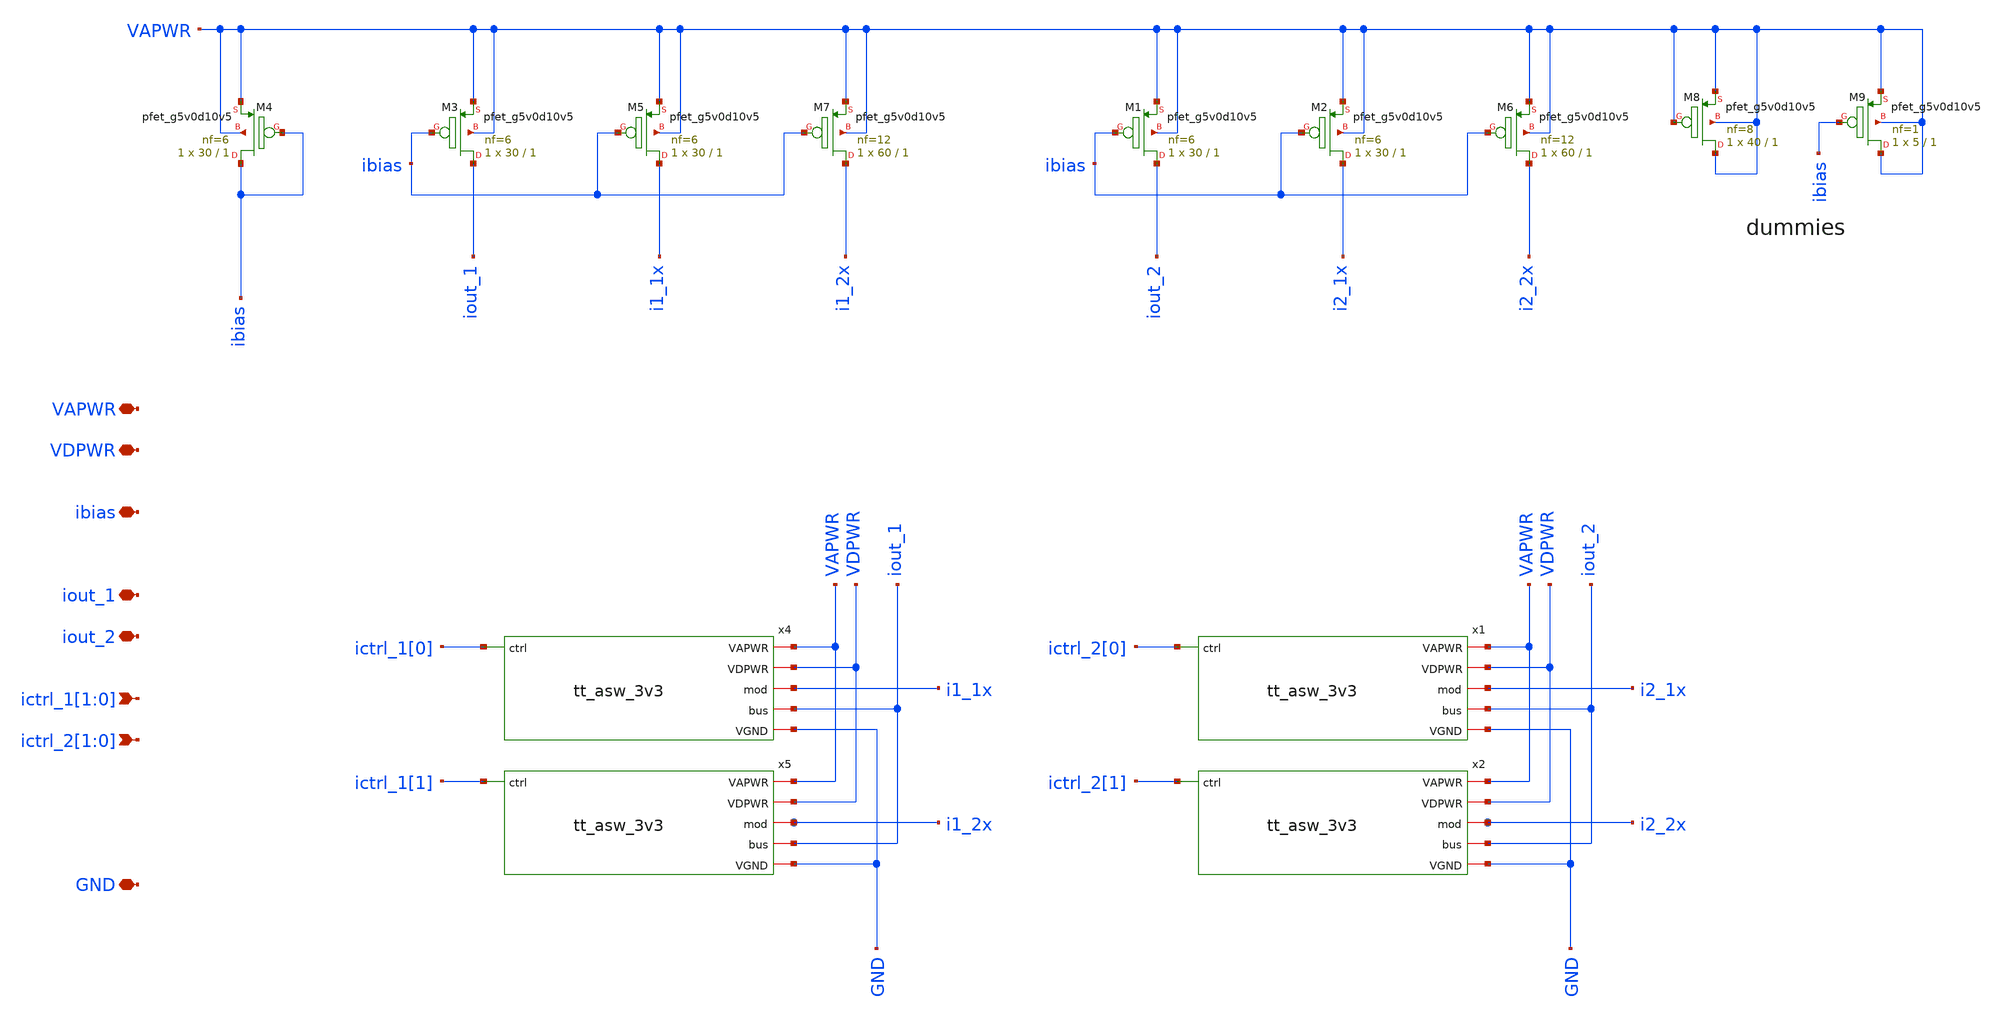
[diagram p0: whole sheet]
** sch_path: tt_um_mosbius/xschem/mirror_p.sch
**.subckt mirror_p ibias iout_1 ictrl_1[1],ictrl_1[0] ictrl_2[1],ictrl_2[0] iout_2 VAPWR VDPWR GND
*.iopin ibias
*.iopin iout_1
*.ipin ictrl_1[1],ictrl_1[0]
*.ipin ictrl_2[1],ictrl_2[0]
*.iopin iout_2
*.iopin VAPWR
*.iopin VDPWR
*.iopin GND
x4 GND VDPWR VAPWR ictrl_1[0] i1_1x iout_1 tt_asw_3v3
x5 GND VDPWR VAPWR ictrl_1[1] i1_2x iout_1 tt_asw_3v3
x1 GND VDPWR VAPWR ictrl_2[0] i2_1x iout_2 tt_asw_3v3
x2 GND VDPWR VAPWR ictrl_2[1] i2_2x iout_2 tt_asw_3v3
XM3 iout_1 ibias VAPWR VAPWR sky130_fd_pr__pfet_g5v0d10v5 L=1 W=30 nf=6 ad='int((nf+1)/2) * W/nf * 0.29'
+ as='int((nf+2)/2) * W/nf * 0.29' pd='2*int((nf+1)/2) * (W/nf + 0.29)' ps='2*int((nf+2)/2) * (W/nf + 0.29)'
+ nrd='0.29 / W' nrs='0.29 / W' sa=0 sb=0 sd=0 mult=1 m=1
XM4 ibias ibias VAPWR VAPWR sky130_fd_pr__pfet_g5v0d10v5 L=1 W=30 nf=6 ad='int((nf+1)/2) * W/nf * 0.29'
+ as='int((nf+2)/2) * W/nf * 0.29' pd='2*int((nf+1)/2) * (W/nf + 0.29)' ps='2*int((nf+2)/2) * (W/nf + 0.29)'
+ nrd='0.29 / W' nrs='0.29 / W' sa=0 sb=0 sd=0 mult=1 m=1
XM5 i1_1x ibias VAPWR VAPWR sky130_fd_pr__pfet_g5v0d10v5 L=1 W=30 nf=6 ad='int((nf+1)/2) * W/nf * 0.29'
+ as='int((nf+2)/2) * W/nf * 0.29' pd='2*int((nf+1)/2) * (W/nf + 0.29)' ps='2*int((nf+2)/2) * (W/nf + 0.29)'
+ nrd='0.29 / W' nrs='0.29 / W' sa=0 sb=0 sd=0 mult=1 m=1
XM7 i1_2x ibias VAPWR VAPWR sky130_fd_pr__pfet_g5v0d10v5 L=1 W=60 nf=12 ad='int((nf+1)/2) * W/nf * 0.29'
+ as='int((nf+2)/2) * W/nf * 0.29' pd='2*int((nf+1)/2) * (W/nf + 0.29)' ps='2*int((nf+2)/2) * (W/nf + 0.29)'
+ nrd='0.29 / W' nrs='0.29 / W' sa=0 sb=0 sd=0 mult=1 m=1
XM1 iout_2 ibias VAPWR VAPWR sky130_fd_pr__pfet_g5v0d10v5 L=1 W=30 nf=6 ad='int((nf+1)/2) * W/nf * 0.29'
+ as='int((nf+2)/2) * W/nf * 0.29' pd='2*int((nf+1)/2) * (W/nf + 0.29)' ps='2*int((nf+2)/2) * (W/nf + 0.29)'
+ nrd='0.29 / W' nrs='0.29 / W' sa=0 sb=0 sd=0 mult=1 m=1
XM2 i2_1x ibias VAPWR VAPWR sky130_fd_pr__pfet_g5v0d10v5 L=1 W=30 nf=6 ad='int((nf+1)/2) * W/nf * 0.29'
+ as='int((nf+2)/2) * W/nf * 0.29' pd='2*int((nf+1)/2) * (W/nf + 0.29)' ps='2*int((nf+2)/2) * (W/nf + 0.29)'
+ nrd='0.29 / W' nrs='0.29 / W' sa=0 sb=0 sd=0 mult=1 m=1
XM6 i2_2x ibias VAPWR VAPWR sky130_fd_pr__pfet_g5v0d10v5 L=1 W=60 nf=12 ad='int((nf+1)/2) * W/nf * 0.29'
+ as='int((nf+2)/2) * W/nf * 0.29' pd='2*int((nf+1)/2) * (W/nf + 0.29)' ps='2*int((nf+2)/2) * (W/nf + 0.29)'
+ nrd='0.29 / W' nrs='0.29 / W' sa=0 sb=0 sd=0 mult=1 m=1
XM8 VAPWR VAPWR VAPWR VAPWR sky130_fd_pr__pfet_g5v0d10v5 L=1 W=40 nf=8 ad='int((nf+1)/2) * W/nf * 0.29'
+ as='int((nf+2)/2) * W/nf * 0.29' pd='2*int((nf+1)/2) * (W/nf + 0.29)' ps='2*int((nf+2)/2) * (W/nf + 0.29)'
+ nrd='0.29 / W' nrs='0.29 / W' sa=0 sb=0 sd=0 mult=1 m=1
XM9 VAPWR ibias VAPWR VAPWR sky130_fd_pr__pfet_g5v0d10v5 L=1 W=5 nf=1 ad='int((nf+1)/2) * W/nf * 0.29'
+ as='int((nf+2)/2) * W/nf * 0.29' pd='2*int((nf+1)/2) * (W/nf + 0.29)' ps='2*int((nf+2)/2) * (W/nf + 0.29)'
+ nrd='0.29 / W' nrs='0.29 / W' sa=0 sb=0 sd=0 mult=1 m=1
**.ends

* expanding   symbol:  tt_asw_3v3.sym # of pins=6
** sym_path: tt_asw_3v3.sym
** sch_path: tt_asw_3v3.sch
.subckt tt_asw_3v3 VGND VDPWR VAPWR ctrl mod bus
*.iopin mod
*.iopin bus
*.ipin ctrl
*.iopin VGND
*.iopin VDPWR
*.iopin VAPWR
XM1 tgon_n net2 VAPWR VAPWR sky130_fd_pr__pfet_g5v0d10v5 L=0.5 W=0.84 nf=1 ad='int((nf+1)/2) * W/nf * 0.29'
+ as='int((nf+2)/2) * W/nf * 0.29' pd='2*int((nf+1)/2) * (W/nf + 0.29)' ps='2*int((nf+2)/2) * (W/nf + 0.29)'
+ nrd='0.29 / W' nrs='0.29 / W' sa=0 sb=0 sd=0 mult=1 m=1
XM2 tgon_n net2 VGND VGND sky130_fd_pr__nfet_g5v0d10v5 L=0.5 W=0.42 nf=1 ad='int((nf+1)/2) * W/nf * 0.29'
+ as='int((nf+2)/2) * W/nf * 0.29' pd='2*int((nf+1)/2) * (W/nf + 0.29)' ps='2*int((nf+2)/2) * (W/nf + 0.29)'
+ nrd='0.29 / W' nrs='0.29 / W' sa=0 sb=0 sd=0 mult=1 m=1
XM3 tgon net1 VAPWR VAPWR sky130_fd_pr__pfet_g5v0d10v5 L=0.5 W=0.84 nf=1 ad='int((nf+1)/2) * W/nf * 0.29'
+ as='int((nf+2)/2) * W/nf * 0.29' pd='2*int((nf+1)/2) * (W/nf + 0.29)' ps='2*int((nf+2)/2) * (W/nf + 0.29)'
+ nrd='0.29 / W' nrs='0.29 / W' sa=0 sb=0 sd=0 mult=1 m=1
XM4 tgon net1 VGND VGND sky130_fd_pr__nfet_g5v0d10v5 L=0.5 W=0.42 nf=1 ad='int((nf+1)/2) * W/nf * 0.29'
+ as='int((nf+2)/2) * W/nf * 0.29' pd='2*int((nf+1)/2) * (W/nf + 0.29)' ps='2*int((nf+2)/2) * (W/nf + 0.29)'
+ nrd='0.29 / W' nrs='0.29 / W' sa=0 sb=0 sd=0 mult=1 m=1
XM5 bus tgon_n mod VAPWR sky130_fd_pr__pfet_g5v0d10v5 L=0.5 W=180 nf=18 ad='int((nf+1)/2) * W/nf * 0.29'
+ as='int((nf+2)/2) * W/nf * 0.29' pd='2*int((nf+1)/2) * (W/nf + 0.29)' ps='2*int((nf+2)/2) * (W/nf + 0.29)'
+ nrd='0.29 / W' nrs='0.29 / W' sa=0 sb=0 sd=0 mult=1 m=1
XM6 bus tgon mod VGND sky130_fd_pr__nfet_g5v0d10v5 L=0.5 W=60 nf=12 ad='int((nf+1)/2) * W/nf * 0.29'
+ as='int((nf+2)/2) * W/nf * 0.29' pd='2*int((nf+1)/2) * (W/nf + 0.29)' ps='2*int((nf+2)/2) * (W/nf + 0.29)'
+ nrd='0.29 / W' nrs='0.29 / W' sa=0 sb=0 sd=0 mult=1 m=1
XM7 ctrl_n ctrl VGND VGND sky130_fd_pr__nfet_01v8 L=0.15 W=0.42 nf=1 ad='int((nf+1)/2) * W/nf * 0.29'
+ as='int((nf+2)/2) * W/nf * 0.29' pd='2*int((nf+1)/2) * (W/nf + 0.29)' ps='2*int((nf+2)/2) * (W/nf + 0.29)'
+ nrd='0.29 / W' nrs='0.29 / W' sa=0 sb=0 sd=0 mult=1 m=1
XM8 ctrl_n ctrl VDPWR VDPWR sky130_fd_pr__pfet_01v8_hvt L=0.15 W=1 nf=1 ad='int((nf+1)/2) * W/nf * 0.29'
+ as='int((nf+2)/2) * W/nf * 0.29' pd='2*int((nf+1)/2) * (W/nf + 0.29)' ps='2*int((nf+2)/2) * (W/nf + 0.29)'
+ nrd='0.29 / W' nrs='0.29 / W' sa=0 sb=0 sd=0 mult=1 m=1
XM9 net1 ctrl VGND VGND sky130_fd_pr__nfet_g5v0d10v5 L=0.5 W=0.42 nf=1 ad='int((nf+1)/2) * W/nf * 0.29'
+ as='int((nf+2)/2) * W/nf * 0.29' pd='2*int((nf+1)/2) * (W/nf + 0.29)' ps='2*int((nf+2)/2) * (W/nf + 0.29)'
+ nrd='0.29 / W' nrs='0.29 / W' sa=0 sb=0 sd=0 mult=1 m=1
XM10 net2 ctrl_n VGND VGND sky130_fd_pr__nfet_g5v0d10v5 L=0.5 W=0.42 nf=1 ad='int((nf+1)/2) * W/nf * 0.29'
+ as='int((nf+2)/2) * W/nf * 0.29' pd='2*int((nf+1)/2) * (W/nf + 0.29)' ps='2*int((nf+2)/2) * (W/nf + 0.29)'
+ nrd='0.29 / W' nrs='0.29 / W' sa=0 sb=0 sd=0 mult=1 m=1
XM11 net1 net2 net3 VAPWR sky130_fd_pr__pfet_g5v0d10v5 L=0.5 W=0.42 nf=1 ad='int((nf+1)/2) * W/nf * 0.29'
+ as='int((nf+2)/2) * W/nf * 0.29' pd='2*int((nf+1)/2) * (W/nf + 0.29)' ps='2*int((nf+2)/2) * (W/nf + 0.29)'
+ nrd='0.29 / W' nrs='0.29 / W' sa=0 sb=0 sd=0 mult=1 m=1
XM12 net2 net1 net4 VAPWR sky130_fd_pr__pfet_g5v0d10v5 L=0.5 W=0.42 nf=1 ad='int((nf+1)/2) * W/nf * 0.29'
+ as='int((nf+2)/2) * W/nf * 0.29' pd='2*int((nf+1)/2) * (W/nf + 0.29)' ps='2*int((nf+2)/2) * (W/nf + 0.29)'
+ nrd='0.29 / W' nrs='0.29 / W' sa=0 sb=0 sd=0 mult=1 m=1
XM13 net3 net1 VAPWR VAPWR sky130_fd_pr__pfet_g5v0d10v5 L=0.5 W=0.42 nf=1 ad='int((nf+1)/2) * W/nf * 0.29'
+ as='int((nf+2)/2) * W/nf * 0.29' pd='2*int((nf+1)/2) * (W/nf + 0.29)' ps='2*int((nf+2)/2) * (W/nf + 0.29)'
+ nrd='0.29 / W' nrs='0.29 / W' sa=0 sb=0 sd=0 mult=1 m=1
XM14 net4 net2 VAPWR VAPWR sky130_fd_pr__pfet_g5v0d10v5 L=0.5 W=0.42 nf=1 ad='int((nf+1)/2) * W/nf * 0.29'
+ as='int((nf+2)/2) * W/nf * 0.29' pd='2*int((nf+1)/2) * (W/nf + 0.29)' ps='2*int((nf+2)/2) * (W/nf + 0.29)'
+ nrd='0.29 / W' nrs='0.29 / W' sa=0 sb=0 sd=0 mult=1 m=1
.ends

.end
